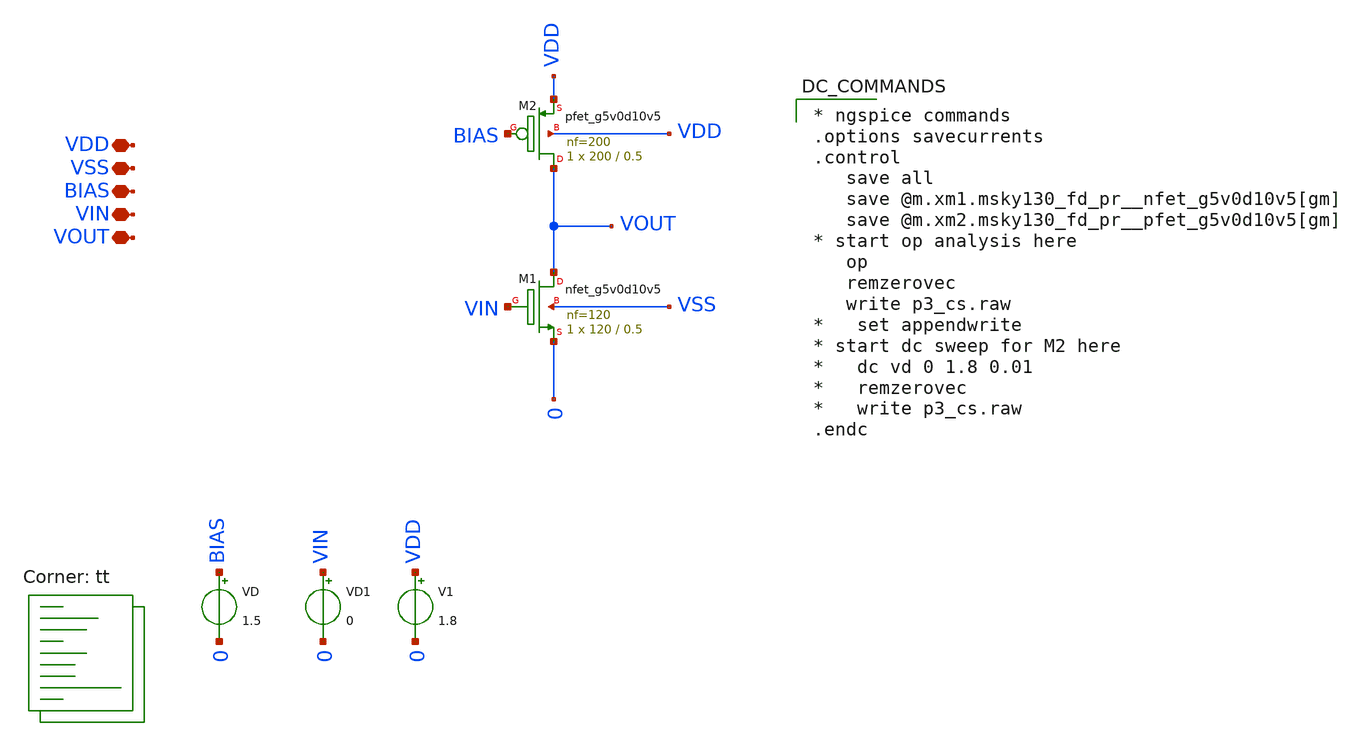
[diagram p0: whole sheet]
** sch_path: xschem/p3_cs.sch
**.subckt p3_cs VDD VSS BIAS VIN VOUT
*.iopin VDD
*.iopin VSS
*.iopin BIAS
*.iopin VIN
*.iopin VOUT
XM2 VOUT BIAS VDD VDD sky130_fd_pr__pfet_g5v0d10v5 L=0.5 W=200 nf=200 ad='int((nf+1)/2) * W/nf * 0.29'
+ as='int((nf+2)/2) * W/nf * 0.29' pd='2*int((nf+1)/2) * (W/nf + 0.29)' ps='2*int((nf+2)/2) * (W/nf + 0.29)'
+ nrd='0.29 / W' nrs='0.29 / W' sa=0 sb=0 sd=0 mult=1 m=1
XM1 VOUT VIN 0 VSS sky130_fd_pr__nfet_g5v0d10v5 L=0.5 W=120 nf=120 ad='int((nf+1)/2) * W/nf * 0.29' as='int((nf+2)/2) * W/nf * 0.29'
+ pd='2*int((nf+1)/2) * (W/nf + 0.29)' ps='2*int((nf+2)/2) * (W/nf + 0.29)' nrd='0.29 / W' nrs='0.29 / W'
+ sa=0 sb=0 sd=0 mult=1 m=1
VD BIAS 0 1.5
V1 VDD 0 1.8
VD1 VIN 0 0
**** begin user architecture code

* ngspice commands
.options savecurrents
.control
   save all
   save @m.xm1.msky130_fd_pr__nfet_g5v0d10v5[gm]
   save @m.xm2.msky130_fd_pr__pfet_g5v0d10v5[gm]
* start op analysis here
   op
   remzerovec
   write p3_cs.raw
*   set appendwrite
* start dc sweep for M2 here
*   dc vd 0 1.8 0.01
*   remzerovec
*   write p3_cs.raw
.endc


.lib $::SKYWATER_MODELS/sky130.lib.spice tt
**** end user architecture code
**.ends
.end
